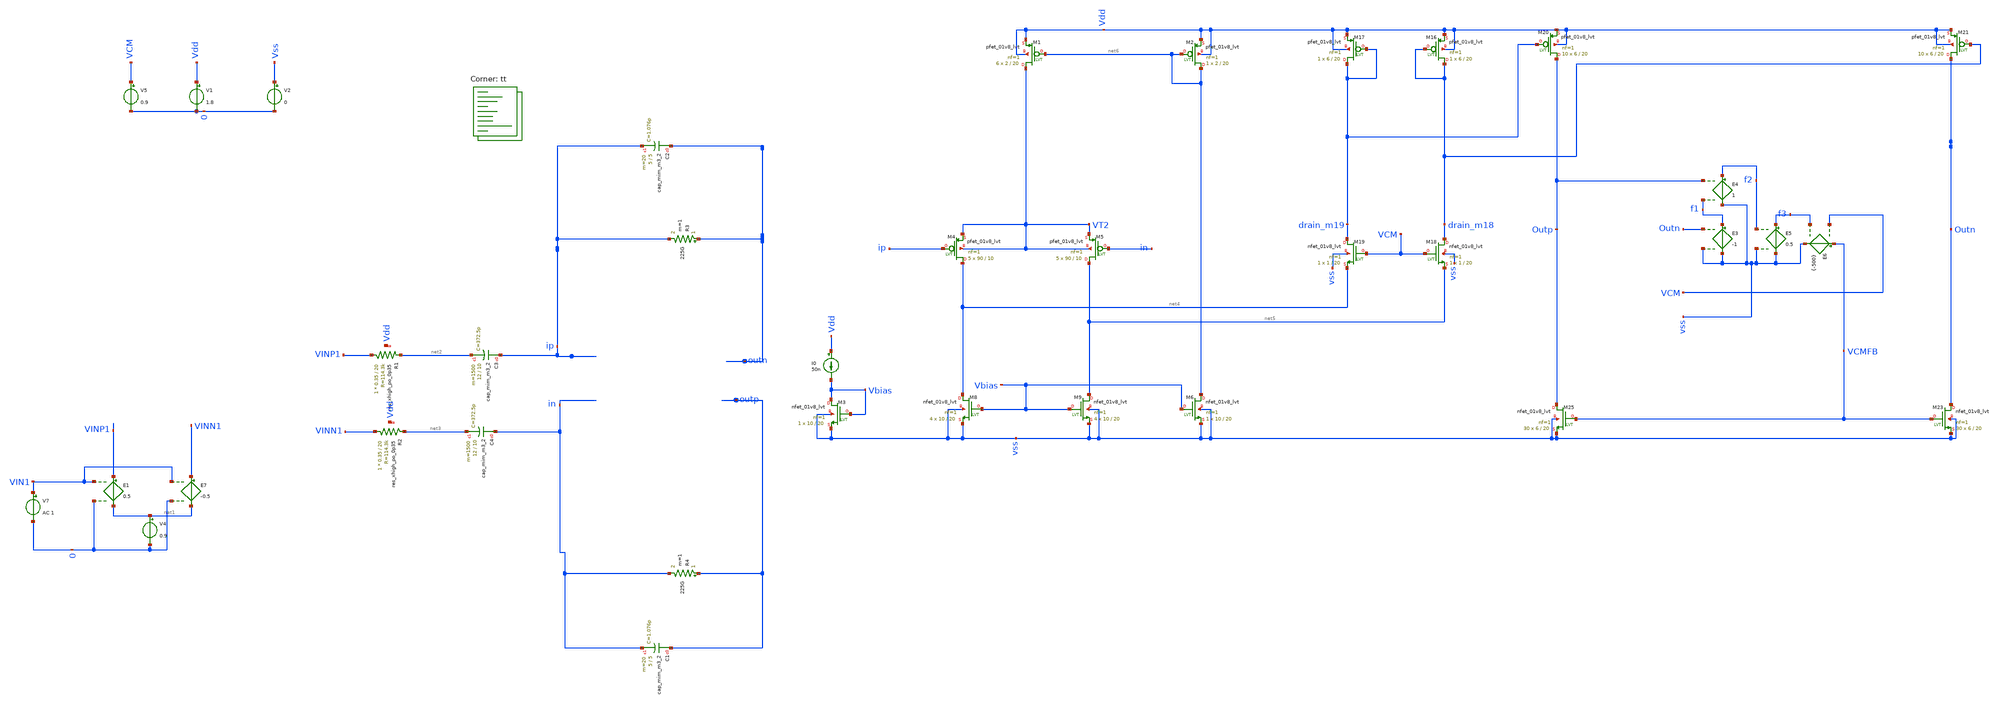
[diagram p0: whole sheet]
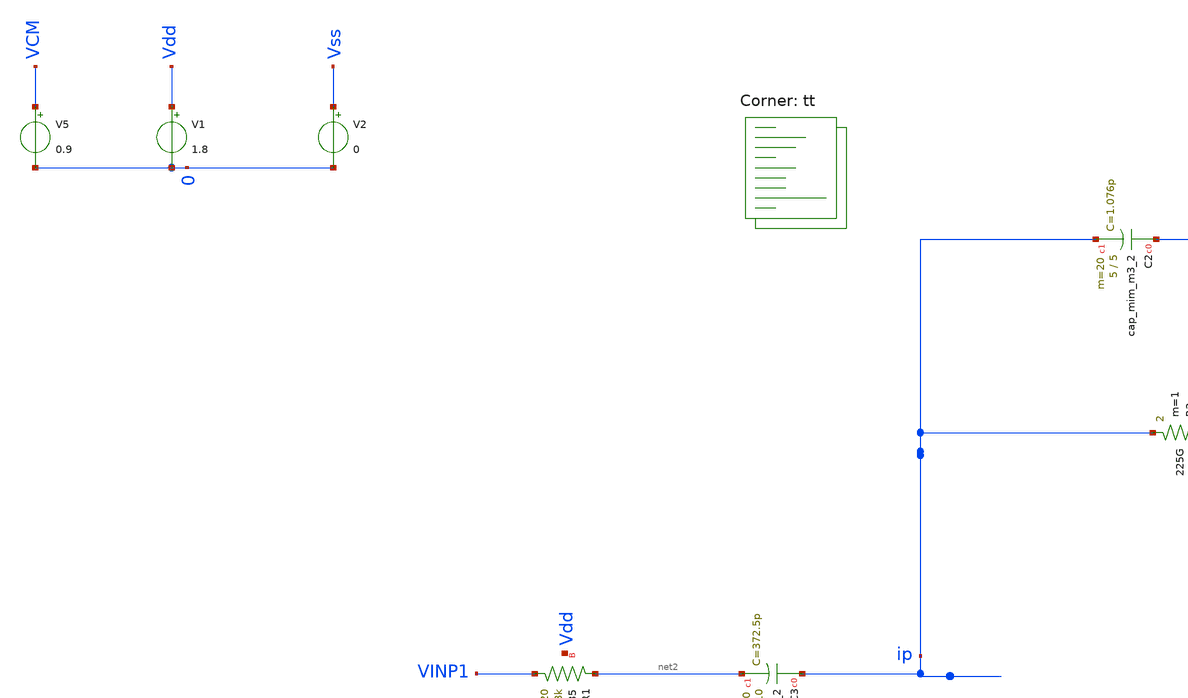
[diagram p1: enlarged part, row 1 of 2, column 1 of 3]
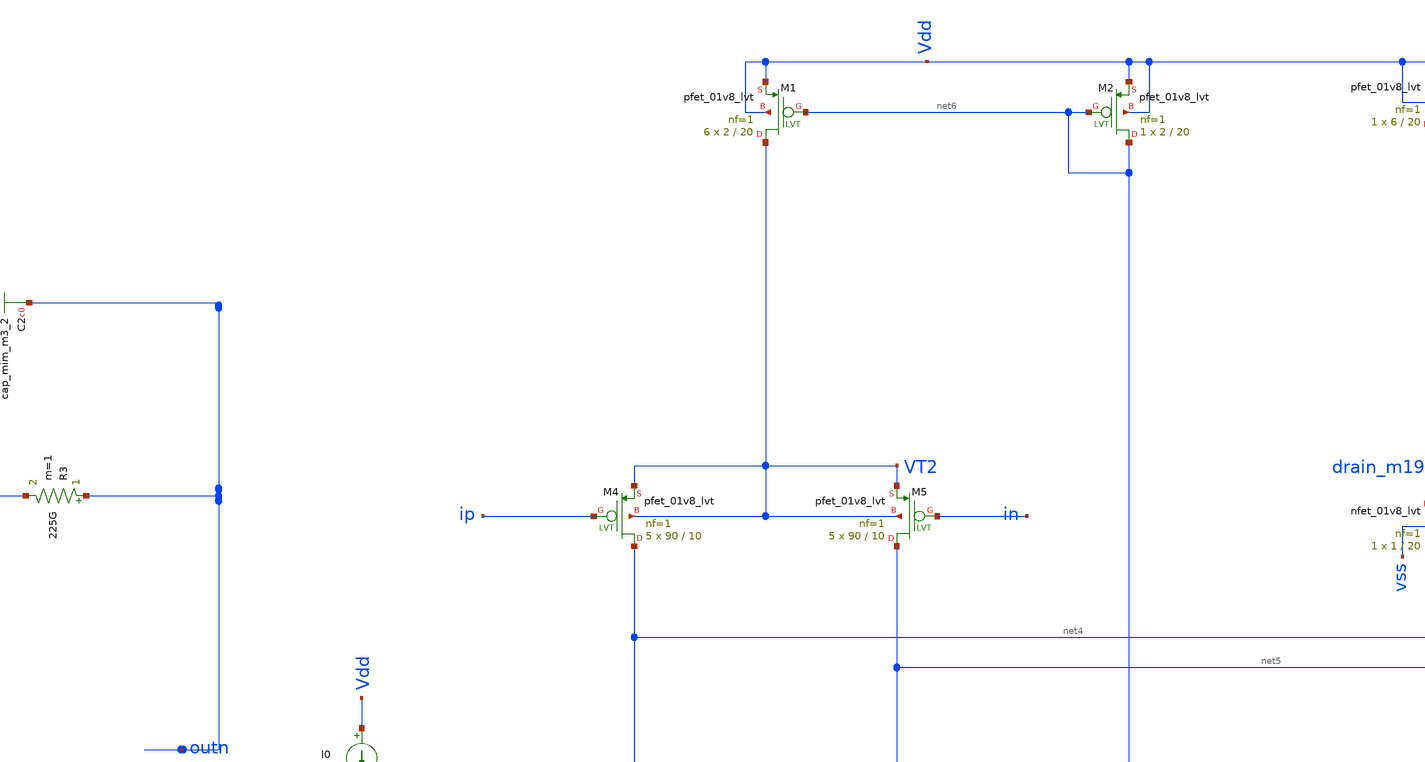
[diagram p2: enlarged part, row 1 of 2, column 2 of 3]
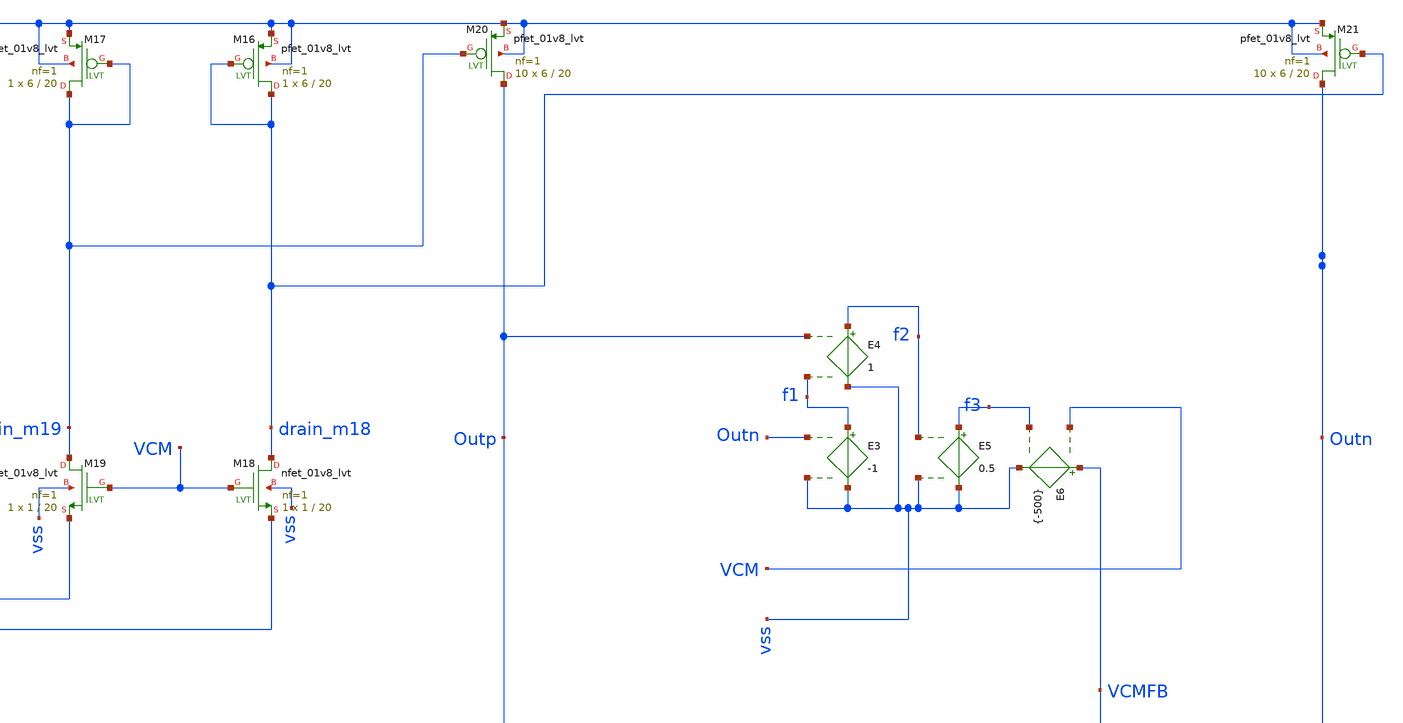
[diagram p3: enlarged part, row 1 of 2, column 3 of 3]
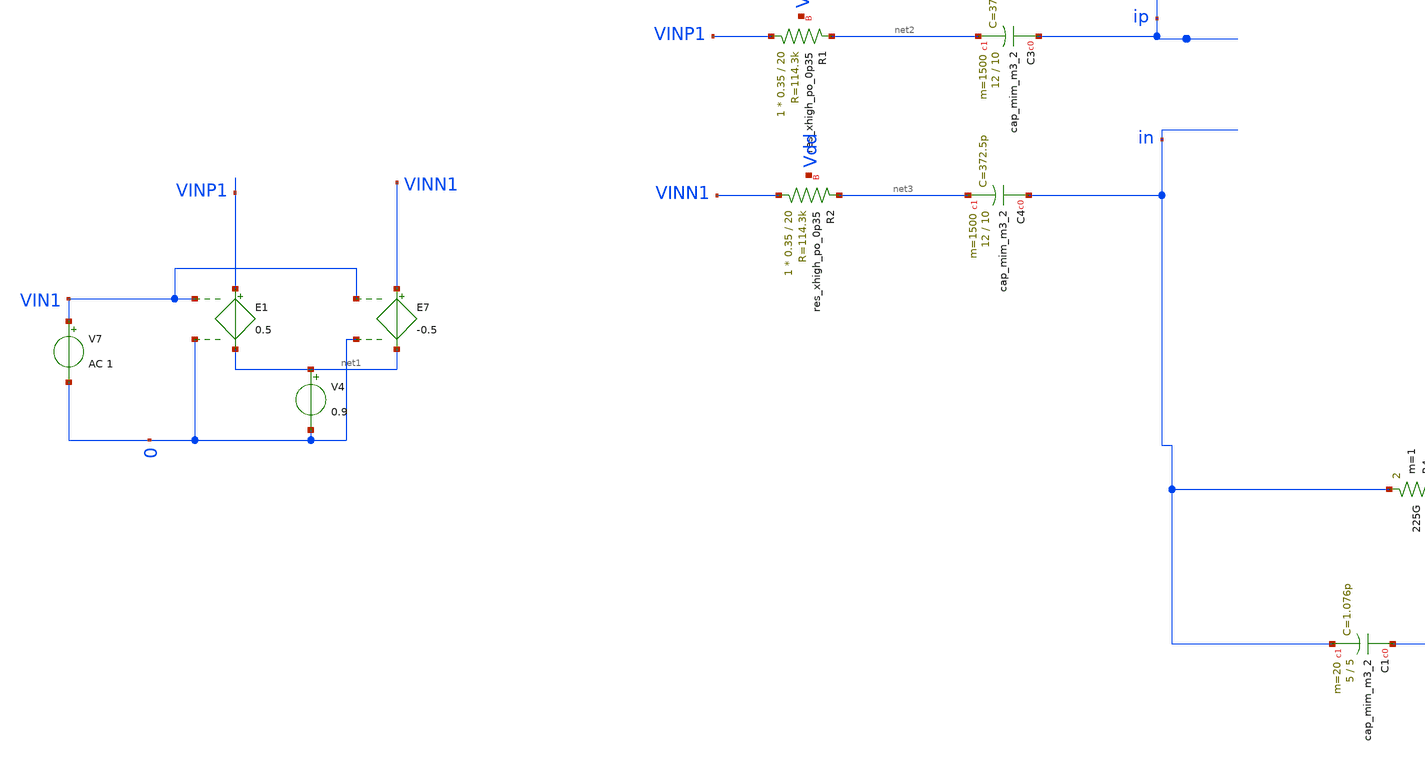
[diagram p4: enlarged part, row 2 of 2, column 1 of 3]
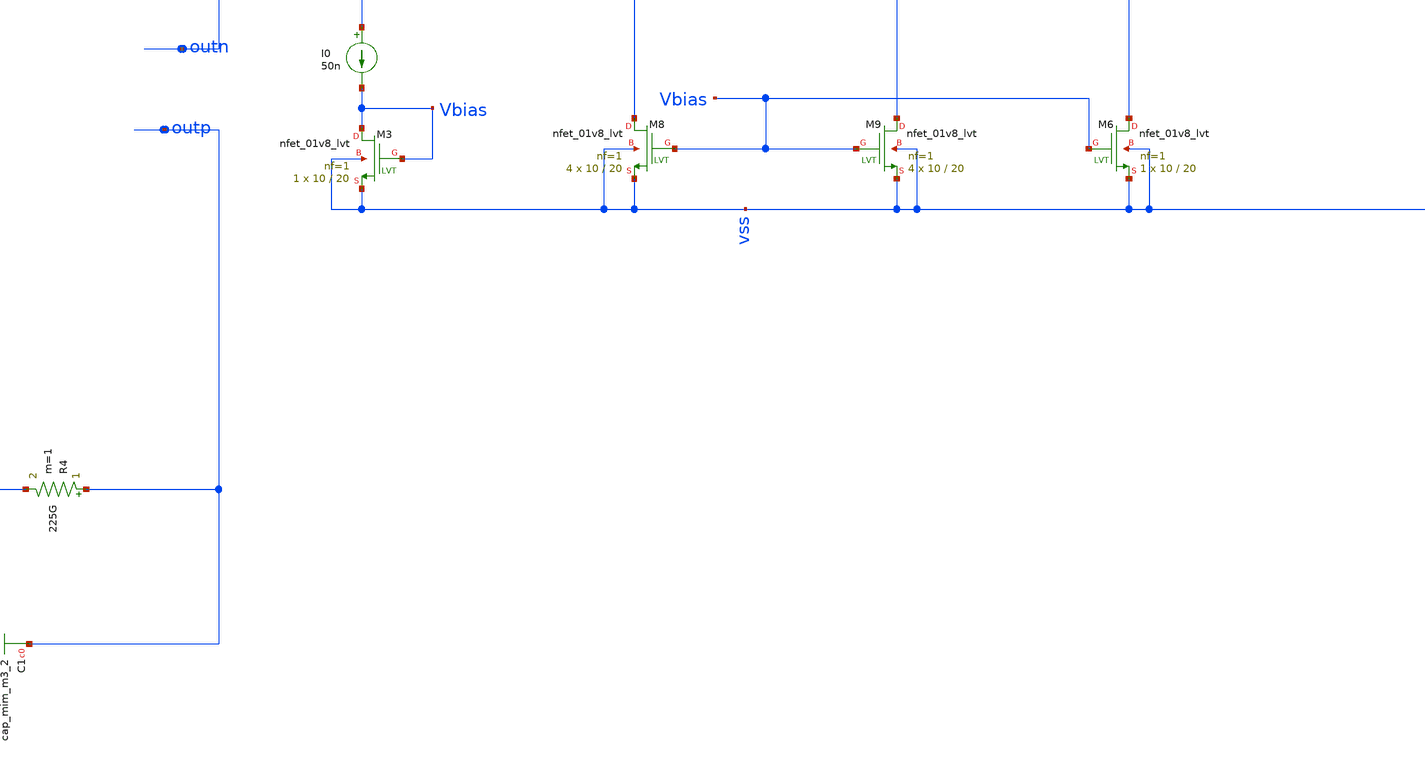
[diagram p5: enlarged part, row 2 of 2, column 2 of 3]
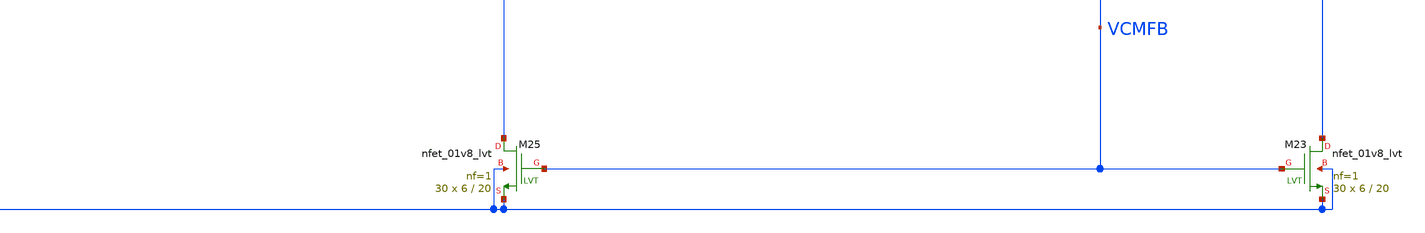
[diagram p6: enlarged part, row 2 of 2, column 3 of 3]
** sch_path: testbench.sch
**.subckt testbench
E1 VINP1 net1 VIN1 0 0.5
E7 VINN1 net1 VIN1 0 -0.5
V4 net1 0 0.9
V1 Vdd 0 1.8
V2 Vss 0 0
V5 VCM 0 0.9
XC1 outp in sky130_fd_pr__cap_mim_m3_2 W=5 L=5 MF=20 m=20
XC2 outn ip sky130_fd_pr__cap_mim_m3_2 W=5 L=5 MF=20 m=20
XC3 ip net2 sky130_fd_pr__cap_mim_m3_2 W=12 L=10 MF=1500 m=1500
XC4 in net3 sky130_fd_pr__cap_mim_m3_2 W=12 L=10 MF=1500 m=1500
V7 VIN1 0 AC 1
XM4 net4 ip VT2 VT2 sky130_fd_pr__pfet_01v8_lvt L=10 W=90 nf=1 ad='int((nf+1)/2) * W/nf * 0.29' as='int((nf+2)/2) * W/nf * 0.29'
+ pd='2*int((nf+1)/2) * (W/nf + 0.29)' ps='2*int((nf+2)/2) * (W/nf + 0.29)' nrd='0.29 / W' nrs='0.29 / W'
+ sa=0 sb=0 sd=0 mult=5 m=5
XM5 net5 in VT2 VT2 sky130_fd_pr__pfet_01v8_lvt L=10 W=90 nf=1 ad='int((nf+1)/2) * W/nf * 0.29' as='int((nf+2)/2) * W/nf * 0.29'
+ pd='2*int((nf+1)/2) * (W/nf + 0.29)' ps='2*int((nf+2)/2) * (W/nf + 0.29)' nrd='0.29 / W' nrs='0.29 / W'
+ sa=0 sb=0 sd=0 mult=5 m=5
XM8 net4 Vbias vss vss sky130_fd_pr__nfet_01v8_lvt L=20 W=10 nf=1 ad='int((nf+1)/2) * W/nf * 0.29' as='int((nf+2)/2) * W/nf * 0.29'
+ pd='2*int((nf+1)/2) * (W/nf + 0.29)' ps='2*int((nf+2)/2) * (W/nf + 0.29)' nrd='0.29 / W' nrs='0.29 / W'
+ sa=0 sb=0 sd=0 mult=4 m=4
XM9 net5 Vbias vss vss sky130_fd_pr__nfet_01v8_lvt L=20 W=10 nf=1 ad='int((nf+1)/2) * W/nf * 0.29' as='int((nf+2)/2) * W/nf * 0.29'
+ pd='2*int((nf+1)/2) * (W/nf + 0.29)' ps='2*int((nf+2)/2) * (W/nf + 0.29)' nrd='0.29 / W' nrs='0.29 / W'
+ sa=0 sb=0 sd=0 mult=4 m=4
XM16 drain_m18 drain_m18 Vdd Vdd sky130_fd_pr__pfet_01v8_lvt L=20 W=6 nf=1 ad='int((nf+1)/2) * W/nf * 0.29'
+ as='int((nf+2)/2) * W/nf * 0.29' pd='2*int((nf+1)/2) * (W/nf + 0.29)' ps='2*int((nf+2)/2) * (W/nf + 0.29)'
+ nrd='0.29 / W' nrs='0.29 / W' sa=0 sb=0 sd=0 mult=1 m=1
XM17 drain_m19 drain_m19 Vdd Vdd sky130_fd_pr__pfet_01v8_lvt L=20 W=6 nf=1 ad='int((nf+1)/2) * W/nf * 0.29'
+ as='int((nf+2)/2) * W/nf * 0.29' pd='2*int((nf+1)/2) * (W/nf + 0.29)' ps='2*int((nf+2)/2) * (W/nf + 0.29)'
+ nrd='0.29 / W' nrs='0.29 / W' sa=0 sb=0 sd=0 mult=1 m=1
XM18 drain_m18 VCM net5 vss sky130_fd_pr__nfet_01v8_lvt L=20 W=1 nf=1 ad='int((nf+1)/2) * W/nf * 0.29'
+ as='int((nf+2)/2) * W/nf * 0.29' pd='2*int((nf+1)/2) * (W/nf + 0.29)' ps='2*int((nf+2)/2) * (W/nf + 0.29)'
+ nrd='0.29 / W' nrs='0.29 / W' sa=0 sb=0 sd=0 mult=1 m=1
XM19 drain_m19 VCM net4 vss sky130_fd_pr__nfet_01v8_lvt L=20 W=1 nf=1 ad='int((nf+1)/2) * W/nf * 0.29'
+ as='int((nf+2)/2) * W/nf * 0.29' pd='2*int((nf+1)/2) * (W/nf + 0.29)' ps='2*int((nf+2)/2) * (W/nf + 0.29)'
+ nrd='0.29 / W' nrs='0.29 / W' sa=0 sb=0 sd=0 mult=1 m=1
XM20 Outp drain_m19 Vdd Vdd sky130_fd_pr__pfet_01v8_lvt L=20 W=6 nf=1 ad='int((nf+1)/2) * W/nf * 0.29'
+ as='int((nf+2)/2) * W/nf * 0.29' pd='2*int((nf+1)/2) * (W/nf + 0.29)' ps='2*int((nf+2)/2) * (W/nf + 0.29)'
+ nrd='0.29 / W' nrs='0.29 / W' sa=0 sb=0 sd=0 mult=10 m=10
XM21 Outn drain_m18 Vdd Vdd sky130_fd_pr__pfet_01v8_lvt L=20 W=6 nf=1 ad='int((nf+1)/2) * W/nf * 0.29'
+ as='int((nf+2)/2) * W/nf * 0.29' pd='2*int((nf+1)/2) * (W/nf + 0.29)' ps='2*int((nf+2)/2) * (W/nf + 0.29)'
+ nrd='0.29 / W' nrs='0.29 / W' sa=0 sb=0 sd=0 mult=10 m=10
XM23 Outn VCMFB vss vss sky130_fd_pr__nfet_01v8_lvt L=20 W=6 nf=1 ad='int((nf+1)/2) * W/nf * 0.29' as='int((nf+2)/2) * W/nf * 0.29'
+ pd='2*int((nf+1)/2) * (W/nf + 0.29)' ps='2*int((nf+2)/2) * (W/nf + 0.29)' nrd='0.29 / W' nrs='0.29 / W'
+ sa=0 sb=0 sd=0 mult=30 m=30
XM25 Outp VCMFB vss vss sky130_fd_pr__nfet_01v8_lvt L=20 W=6 nf=1 ad='int((nf+1)/2) * W/nf * 0.29' as='int((nf+2)/2) * W/nf * 0.29'
+ pd='2*int((nf+1)/2) * (W/nf + 0.29)' ps='2*int((nf+2)/2) * (W/nf + 0.29)' nrd='0.29 / W' nrs='0.29 / W'
+ sa=0 sb=0 sd=0 mult=30 m=30
XM1 VT2 net6 Vdd Vdd sky130_fd_pr__pfet_01v8_lvt L=20 W=2 nf=1 ad='int((nf+1)/2) * W/nf * 0.29' as='int((nf+2)/2) * W/nf * 0.29'
+ pd='2*int((nf+1)/2) * (W/nf + 0.29)' ps='2*int((nf+2)/2) * (W/nf + 0.29)' nrd='0.29 / W' nrs='0.29 / W'
+ sa=0 sb=0 sd=0 mult=6 m=6
XM2 net6 net6 Vdd Vdd sky130_fd_pr__pfet_01v8_lvt L=20 W=2 nf=1 ad='int((nf+1)/2) * W/nf * 0.29' as='int((nf+2)/2) * W/nf * 0.29'
+ pd='2*int((nf+1)/2) * (W/nf + 0.29)' ps='2*int((nf+2)/2) * (W/nf + 0.29)' nrd='0.29 / W' nrs='0.29 / W'
+ sa=0 sb=0 sd=0 mult=1 m=1
I0 Vdd Vbias 50n
XM3 Vbias Vbias vss vss sky130_fd_pr__nfet_01v8_lvt L=20 W=10 nf=1 ad='int((nf+1)/2) * W/nf * 0.29' as='int((nf+2)/2) * W/nf * 0.29'
+ pd='2*int((nf+1)/2) * (W/nf + 0.29)' ps='2*int((nf+2)/2) * (W/nf + 0.29)' nrd='0.29 / W' nrs='0.29 / W'
+ sa=0 sb=0 sd=0 mult=1 m=1
XM6 net6 Vbias vss vss sky130_fd_pr__nfet_01v8_lvt L=20 W=10 nf=1 ad='int((nf+1)/2) * W/nf * 0.29' as='int((nf+2)/2) * W/nf * 0.29'
+ pd='2*int((nf+1)/2) * (W/nf + 0.29)' ps='2*int((nf+2)/2) * (W/nf + 0.29)' nrd='0.29 / W' nrs='0.29 / W'
+ sa=0 sb=0 sd=0 mult=1 m=1
E3 f1 vss Outn vss -1
E4 f2 vss Outp f1 1
E5 f3 vss f2 vss 0.5
E6 VCMFB vss VCM f3 {-500}
R3 outn ip 225G m=1
R4 outp in 225G m=1
XR1 VINP1 net2 Vdd sky130_fd_pr__res_xhigh_po_0p35 L=20 mult=1 m=1
XR2 VINN1 net3 Vdd sky130_fd_pr__res_xhigh_po_0p35 L=20 mult=1 m=1
**** begin user architecture code
.lib $::SKYWATER_MODELS/sky130.lib.spice tt


.options savecurrents
*ic v(VM5)=0.9 v(VM6)=0.9
.control


save all

save @m.xm11.msky130_fd_pr__pfet_01v8_lvt[id]
save @m.xm11.msky130_fd_pr__pfet_01v8_lvt[vgs]


*nmos
save @m.xm3.msky130_fd_pr__nfet_01v8_lvt[vgs]
save @m.xm3.msky130_fd_pr__nfet_01v8_lvt[vth]
save @m.xm3.msky130_fd_pr__nfet_01v8_lvt[vds]

save @m.xm6.msky130_fd_pr__nfet_01v8_lvt[vgs]
save @m.xm6.msky130_fd_pr__nfet_01v8_lvt[vth]
save @m.xm6.msky130_fd_pr__nfet_01v8_lvt[vds]

save @m.xm8.msky130_fd_pr__nfet_01v8_lvt[vgs]
save @m.xm8.msky130_fd_pr__nfet_01v8_lvt[vth]
save @m.xm8.msky130_fd_pr__nfet_01v8_lvt[vds]

save @m.xm9.msky130_fd_pr__nfet_01v8_lvt[vgs]
save @m.xm9.msky130_fd_pr__nfet_01v8_lvt[vth]
save @m.xm9.msky130_fd_pr__nfet_01v8_lvt[vds]

save @m.xm18.msky130_fd_pr__nfet_01v8_lvt[vgs]
save @m.xm18.msky130_fd_pr__nfet_01v8_lvt[vth]
save @m.xm18.msky130_fd_pr__nfet_01v8_lvt[vds]

save @m.xm19.msky130_fd_pr__nfet_01v8_lvt[vgs]
save @m.xm19.msky130_fd_pr__nfet_01v8_lvt[vth]
save @m.xm19.msky130_fd_pr__nfet_01v8_lvt[vds]

save @m.xm25.msky130_fd_pr__nfet_01v8_lvt[vgs]
save @m.xm25.msky130_fd_pr__nfet_01v8_lvt[vth]
save @m.xm25.msky130_fd_pr__nfet_01v8_lvt[vds]

*pmos

save @m.xm1.msky130_fd_pr__pfet_01v8_lvt[vgs]
save @m.xm1.msky130_fd_pr__pfet_01v8_lvt[vth]
save @m.xm1.msky130_fd_pr__pfet_01v8_lvt[vds]


save @m.xm2.msky130_fd_pr__pfet_01v8_lvt[vgs]
save @m.xm2.msky130_fd_pr__pfet_01v8_lvt[vth]
save @m.xm2.msky130_fd_pr__pfet_01v8_lvt[vds]


save @m.xm10.msky130_fd_pr__pfet_01v8_lvt[vgs]
save @m.xm10.msky130_fd_pr__pfet_01v8_lvt[vth]
save @m.xm10.msky130_fd_pr__pfet_01v8_lvt[vds]

save @m.xm13.msky130_fd_pr__pfet_01v8_lvt[vgs]
save @m.xm13.msky130_fd_pr__pfet_01v8_lvt[vth]
save @m.xm13.msky130_fd_pr__pfet_01v8_lvt[vds]

save @m.xm4.msky130_fd_pr__pfet_01v8_lvt[vgs]
save @m.xm4.msky130_fd_pr__pfet_01v8_lvt[vth]
save @m.xm4.msky130_fd_pr__pfet_01v8_lvt[vds]

save @m.xm5.msky130_fd_pr__pfet_01v8_lvt[vgs]
save @m.xm5.msky130_fd_pr__pfet_01v8_lvt[vth]
save @m.xm5.msky130_fd_pr__pfet_01v8_lvt[vds]

save @m.xm16.msky130_fd_pr__pfet_01v8_lvt[vgs]
save @m.xm16.msky130_fd_pr__pfet_01v8_lvt[vth]
save @m.xm16.msky130_fd_pr__pfet_01v8_lvt[vds]

save @m.xm17.msky130_fd_pr__pfet_01v8_lvt[vgs]
save @m.xm17.msky130_fd_pr__pfet_01v8_lvt[vth]
save @m.xm17.msky130_fd_pr__pfet_01v8_lvt[vds]

save @m.xm3.msky130_fd_pr__pfet_01v8_lvt[vgs]
save @m.xm3.msky130_fd_pr__pfet_01v8_lvt[vth]
save @m.xm3.msky130_fd_pr__pfet_01v8_lvt[vds]

save @m.xm20.msky130_fd_pr__pfet_01v8_lvt[vgs]
save @m.xm20.msky130_fd_pr__pfet_01v8_lvt[vth]
save @m.xm20.msky130_fd_pr__pfet_01v8_lvt[vds]

save @m.xm2.msky130_fd_pr__pfet_01v8_lvt[vgs]
save @m.xm2.msky130_fd_pr__pfet_01v8_lvt[vth]
save @m.xm2.msky130_fd_pr__pfet_01v8_lvt[vds]

save @m.xm21.msky130_fd_pr__pfet_01v8_lvt[vgs]
save @m.xm21.msky130_fd_pr__pfet_01v8_lvt[vth]
save @m.xm21.msky130_fd_pr__pfet_01v8_lvt[vds]

save @m.xm7.msky130_fd_pr__nfet_01v8_lvt[vth]

save @m.xm1.msky130_fd_pr__pfet_01v8[vgs]

save @m.xm1.msky130_fd_pr__nfet_01v8_lvt[gm]


save @m.xm1.msky130_fd_pr__nfet_01v8_lvt[gds]
save @m.xm2.msky130_fd_pr__pfet_01v8_lvt[gm]

save @m.xm23.msky130_fd_pr__nfet_01v8[cgs]
save @m.xm4.msky130_fd_pr__pfet_01v8[cgs]
save @m.xm2.msky130_fd_pr__pfet_01v8_lvt[cgs]



save @m.xm2.msky130_fd_pr__pfet_01v8_lvt[gds]


op
write testbench.raw
*set appendwrite


.endc
.control



*tran 50u 1500m
*save all
*plot v(Outp)-v(outn)


noise V(Outp,Outn) V7 dec 100 0.1 128
print inoise_total onoise_total
setplot noise1
plot inoise_spectrum

ac dec 10 0.1 20k
let gaind=(v(outp)-v(outn))/(v(VINP1)-v(VINN1))
plot db(gaind)


.endc






.include $::SKYWATER_STDCELLS/sky130_fd_sc_hd.spice

**** end user architecture code
**.ends
.end
